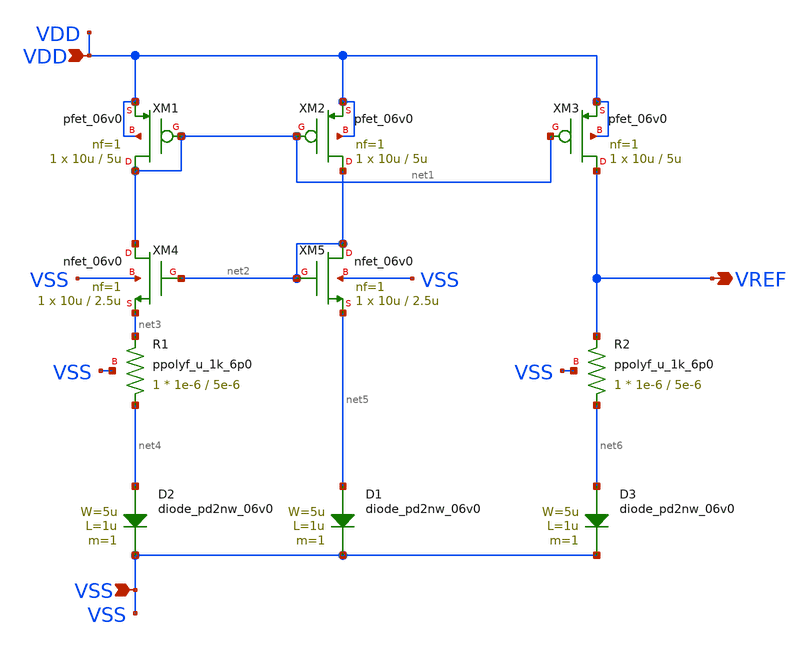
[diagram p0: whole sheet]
** sch_path: analog/xschem/voltage_ref.sch
**.subckt voltage_ref VDD VSS VREF
*.ipin VDD
*.ipin VSS
*.opin VREF
XM1 net1 net1 VDD VDD pfet_06v0 L=5u W=10u nf=1 ad='int((nf+1)/2) * W/nf * 0.18u' as='int((nf+2)/2) * W/nf * 0.18u'
+ pd='2*int((nf+1)/2) * (W/nf + 0.18u)' ps='2*int((nf+2)/2) * (W/nf + 0.18u)' nrd='0.18u / W' nrs='0.18u / W'
+ sa=0 sb=0 sd=0 m=1
XM2 net2 net1 VDD VDD pfet_06v0 L=5u W=10u nf=1 ad='int((nf+1)/2) * W/nf * 0.18u' as='int((nf+2)/2) * W/nf * 0.18u'
+ pd='2*int((nf+1)/2) * (W/nf + 0.18u)' ps='2*int((nf+2)/2) * (W/nf + 0.18u)' nrd='0.18u / W' nrs='0.18u / W'
+ sa=0 sb=0 sd=0 m=1
XM3 VREF net1 VDD VDD pfet_06v0 L=5u W=10u nf=1 ad='int((nf+1)/2) * W/nf * 0.18u' as='int((nf+2)/2) * W/nf * 0.18u'
+ pd='2*int((nf+1)/2) * (W/nf + 0.18u)' ps='2*int((nf+2)/2) * (W/nf + 0.18u)' nrd='0.18u / W' nrs='0.18u / W'
+ sa=0 sb=0 sd=0 m=1
XM4 net1 net2 net3 VSS nfet_06v0 L=2.5u W=10u nf=1 ad='int((nf+1)/2) * W/nf * 0.18u' as='int((nf+2)/2) * W/nf * 0.18u'
+ pd='2*int((nf+1)/2) * (W/nf + 0.18u)' ps='2*int((nf+2)/2) * (W/nf + 0.18u)' nrd='0.18u / W' nrs='0.18u / W'
+ sa=0 sb=0 sd=0 m=1
XM5 net2 net2 net5 VSS nfet_06v0 L=2.5u W=10u nf=1 ad='int((nf+1)/2) * W/nf * 0.18u' as='int((nf+2)/2) * W/nf * 0.18u'
+ pd='2*int((nf+1)/2) * (W/nf + 0.18u)' ps='2*int((nf+2)/2) * (W/nf + 0.18u)' nrd='0.18u / W' nrs='0.18u / W'
+ sa=0 sb=0 sd=0 m=1
XR1 net4 net3 VSS ppolyf_u_1k_6p0 r_width=1e-6 r_length=5e-6 m=1
XR2 net6 VREF VSS ppolyf_u_1k_6p0 r_width=1e-6 r_length=5e-6 m=1
D3 net6 VSS diode_pd2nw_06v0 area='5u * 1u ' pj='2*5u + 2*1u ' m=1
D1 net5 VSS diode_pd2nw_06v0 area='5u * 1u ' pj='2*5u + 2*1u ' m=1
D2 net4 VSS diode_pd2nw_06v0 area='5u * 1u ' pj='2*5u + 2*1u ' m=1
**.ends
.end
